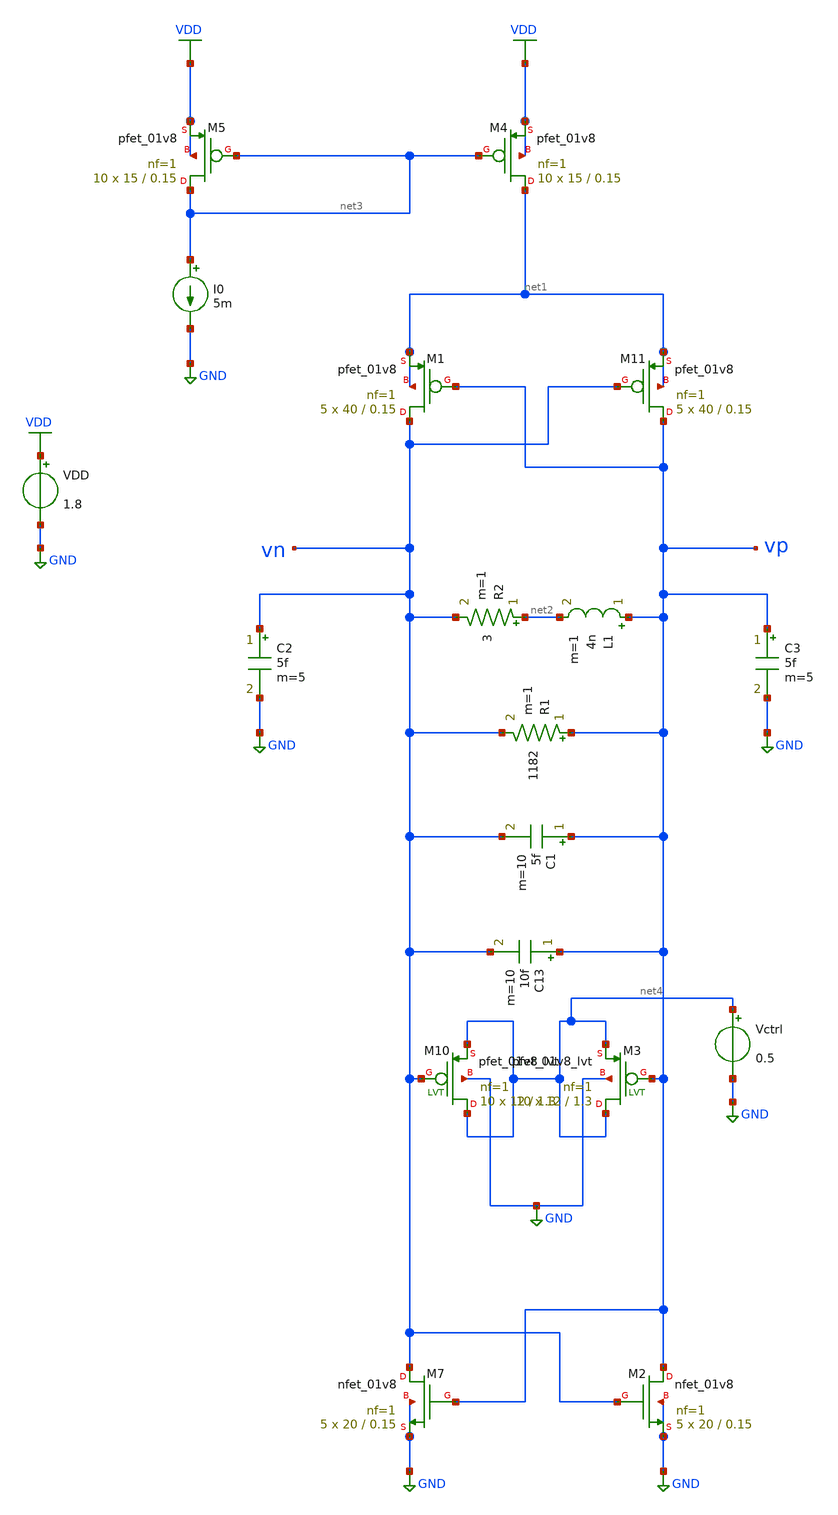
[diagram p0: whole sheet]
** sch_path: pll/lc_vco_lib/Ahmed_Reda/CMOS_LC_VCO/xschem/CMOS_LC_VCO.sch
**.subckt CMOS_LC_VCO
XM11 vp vn net1 net1 sky130_fd_pr__pfet_01v8 L=0.15 W=40 nf=1 ad='int((nf+1)/2) * W/nf * 0.29' as='int((nf+2)/2) * W/nf * 0.29'
+ pd='2*int((nf+1)/2) * (W/nf + 0.29)' ps='2*int((nf+2)/2) * (W/nf + 0.29)' nrd='0.29 / W' nrs='0.29 / W'
+ sa=0 sb=0 sd=0 mult=5 m=5
XM1 vn vp net1 net1 sky130_fd_pr__pfet_01v8 L=0.15 W=40 nf=1 ad='int((nf+1)/2) * W/nf * 0.29' as='int((nf+2)/2) * W/nf * 0.29'
+ pd='2*int((nf+1)/2) * (W/nf + 0.29)' ps='2*int((nf+2)/2) * (W/nf + 0.29)' nrd='0.29 / W' nrs='0.29 / W'
+ sa=0 sb=0 sd=0 mult=5 m=5
XM2 vp vn GND GND sky130_fd_pr__nfet_01v8 L=0.15 W=20 nf=1 ad='int((1 + 1)/2) * 20 / 1 * 0.29' as='int((1 + 2)/2) * 20 / 1 * 0.29'
+ pd='2*int((1 + 1)/2) * (20 / 1 + 0.29)' ps='2*int((1 + 2)/2) * (20 / 1 + 0.29)' nrd='0.29 / 20 ' nrs='0.29 / 20 '
+ sa=0 sb=0 sd=0 mult=5 m=5
L1 vp net2 4n m=1
I0 net3 GND 5m
R1 vp vn 1182 m=1
VDD VDD GND 1.8
R2 net2 vn 3 m=1
XM4 net1 net3 VDD VDD sky130_fd_pr__pfet_01v8 L=0.15 W=15 nf=1 ad='int((nf+1)/2) * W/nf * 0.29' as='int((nf+2)/2) * W/nf * 0.29'
+ pd='2*int((nf+1)/2) * (W/nf + 0.29)' ps='2*int((nf+2)/2) * (W/nf + 0.29)' nrd='0.29 / W' nrs='0.29 / W'
+ sa=0 sb=0 sd=0 mult=10 m=10
XM5 net3 net3 VDD VDD sky130_fd_pr__pfet_01v8 L=0.15 W=15 nf=1 ad='int((nf+1)/2) * W/nf * 0.29' as='int((nf+2)/2) * W/nf * 0.29'
+ pd='2*int((nf+1)/2) * (W/nf + 0.29)' ps='2*int((nf+2)/2) * (W/nf + 0.29)' nrd='0.29 / W' nrs='0.29 / W'
+ sa=0 sb=0 sd=0 mult=10 m=10
XM7 vn vp GND GND sky130_fd_pr__nfet_01v8 L=0.15 W=20 nf=1 ad='int((1 + 1)/2) * 20 / 1 * 0.29' as='int((1 + 2)/2) * 20 / 1 * 0.29'
+ pd='2*int((1 + 1)/2) * (20 / 1 + 0.29)' ps='2*int((1 + 2)/2) * (20 / 1 + 0.29)' nrd='0.29 / 20 ' nrs='0.29 / 20 '
+ sa=0 sb=0 sd=0 mult=5 m=5
C1 vp vn 5f m=10
C3 vp GND 5f m=5
C2 vn GND 5f m=5
Vctrl net4 GND 0.5
XM10 net4 vn net4 GND sky130_fd_pr__pfet_01v8_lvt L=1.3 W=12 nf=1 ad='int((1 + 1)/2) * 12 / 1 * 0.29'
+ as='int((1 + 2)/2) * 12 / 1 * 0.29' pd='2*int((1 + 1)/2) * (12 / 1 + 0.29)' ps='2*int((1 + 2)/2) * (12 / 1 + 0.29)'
+ nrd='0.29 / 12 ' nrs='0.29 / 12 ' sa=0 sb=0 sd=0 mult=10 m=10
XM3 net4 vp net4 GND sky130_fd_pr__pfet_01v8_lvt L=1.3 W=12 nf=1 ad='int((1 + 1)/2) * 12 / 1 * 0.29'
+ as='int((1 + 2)/2) * 12 / 1 * 0.29' pd='2*int((1 + 1)/2) * (12 / 1 + 0.29)' ps='2*int((1 + 2)/2) * (12 / 1 + 0.29)'
+ nrd='0.29 / 12 ' nrs='0.29 / 12 ' sa=0 sb=0 sd=0 mult=10 m=10
C13 vp vn 10f m=10
**.ends
.GLOBAL GND
.GLOBAL VDD
.end
